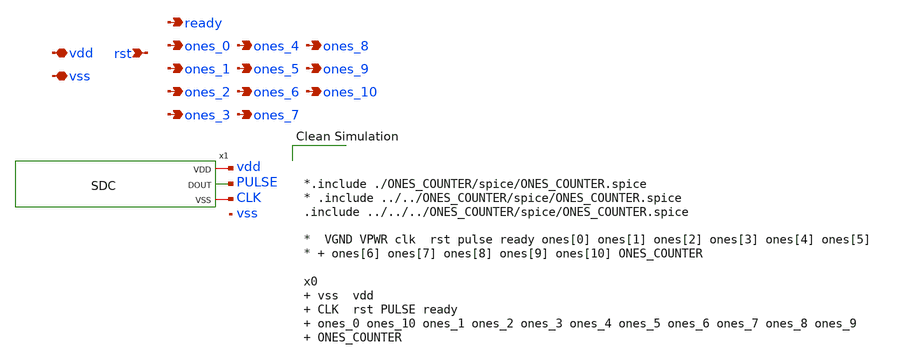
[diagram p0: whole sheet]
** sch_path: modules/SDC_DIGITAL/symbol/SDC_DIGITAL.sch
**.subckt SDC_DIGITAL vdd vss rst ready ones_0 ones_1 ones_2 ones_3 ones_4 ones_5 ones_6 ones_7
*+ ones_8 ones_9 ones_10
*.iopin vdd
*.iopin vss
*.ipin rst
*.opin ready
*.opin ones_0
*.opin ones_1
*.opin ones_2
*.opin ones_3
*.opin ones_4
*.opin ones_5
*.opin ones_6
*.opin ones_7
*.opin ones_8
*.opin ones_9
*.opin ones_10
x1 vdd PULSE CLK SDC
**** begin user architecture code



*.include ./ONES_COUNTER/spice/ONES_COUNTER.spice
* .include ../../ONES_COUNTER/spice/ONES_COUNTER.spice
.include ../../../ONES_COUNTER/spice/ONES_COUNTER.spice

*  VGND VPWR clk  rst pulse ready ones[0] ones[1] ones[2] ones[3] ones[4] ones[5]
* + ones[6] ones[7] ones[8] ones[9] ones[10] ONES_COUNTER

x0   vss  vdd  CLK  rst PULSE ready   ones_0 ones_10 ones_1 ones_2 ones_3 ones_4 ones_5 ones_6
+ ones_7 ones_8 ones_9   ONES_COUNTER


**** end user architecture code
**.ends
.end
